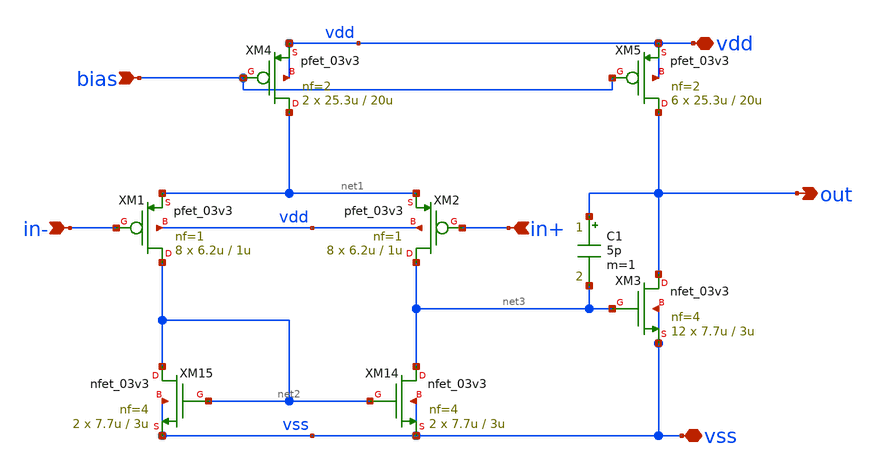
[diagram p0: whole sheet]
** sch_path: design/analog/OTA/two-stage_miller_OTA.sch
**.subckt two-stage_miller_OTA in+ in- out vdd vss bias
*.ipin in+
*.ipin in-
*.opin out
*.iopin vdd
*.iopin vss
*.ipin bias
XM1 net2 in- net1 vdd pfet_03v3 L=1u W=6.2u nf=1 ad='int((nf+1)/2) * W/nf * 0.18u' as='int((nf+2)/2) * W/nf * 0.18u'
+ pd='2*int((nf+1)/2) * (W/nf + 0.18u)' ps='2*int((nf+2)/2) * (W/nf + 0.18u)' nrd='0.18u / W' nrs='0.18u / W'
+ sa=0 sb=0 sd=0 m=8
XM2 net3 in+ net1 vdd pfet_03v3 L=1u W=6.2u nf=1 ad='int((nf+1)/2) * W/nf * 0.18u' as='int((nf+2)/2) * W/nf * 0.18u'
+ pd='2*int((nf+1)/2) * (W/nf + 0.18u)' ps='2*int((nf+2)/2) * (W/nf + 0.18u)' nrd='0.18u / W' nrs='0.18u / W'
+ sa=0 sb=0 sd=0 m=8
XM14 net3 net2 vss vss nfet_03v3 L=3u W=7.7u nf=4 ad='int((nf+1)/2) * W/nf * 0.18u' as='int((nf+2)/2) * W/nf * 0.18u'
+ pd='2*int((nf+1)/2) * (W/nf + 0.18u)' ps='2*int((nf+2)/2) * (W/nf + 0.18u)' nrd='0.18u / W' nrs='0.18u / W'
+ sa=0 sb=0 sd=0 m=2
XM15 net2 net2 vss vss nfet_03v3 L=3u W=7.7u nf=4 ad='int((nf+1)/2) * W/nf * 0.18u' as='int((nf+2)/2) * W/nf * 0.18u'
+ pd='2*int((nf+1)/2) * (W/nf + 0.18u)' ps='2*int((nf+2)/2) * (W/nf + 0.18u)' nrd='0.18u / W' nrs='0.18u / W'
+ sa=0 sb=0 sd=0 m=2
XM3 out net3 vss vss nfet_03v3 L=3u W=7.7u nf=4 ad='int((nf+1)/2) * W/nf * 0.18u' as='int((nf+2)/2) * W/nf * 0.18u'
+ pd='2*int((nf+1)/2) * (W/nf + 0.18u)' ps='2*int((nf+2)/2) * (W/nf + 0.18u)' nrd='0.18u / W' nrs='0.18u / W'
+ sa=0 sb=0 sd=0 m=12
C1 out net3 5p m=1
XM4 net1 bias vdd vdd pfet_03v3 L=20u W=25.3u nf=2 ad='int((nf+1)/2) * W/nf * 0.18u' as='int((nf+2)/2) * W/nf * 0.18u'
+ pd='2*int((nf+1)/2) * (W/nf + 0.18u)' ps='2*int((nf+2)/2) * (W/nf + 0.18u)' nrd='0.18u / W' nrs='0.18u / W'
+ sa=0 sb=0 sd=0 m=2
XM5 out bias vdd vdd pfet_03v3 L=20u W=25.3u nf=2 ad='int((nf+1)/2) * W/nf * 0.18u' as='int((nf+2)/2) * W/nf * 0.18u'
+ pd='2*int((nf+1)/2) * (W/nf + 0.18u)' ps='2*int((nf+2)/2) * (W/nf + 0.18u)' nrd='0.18u / W' nrs='0.18u / W'
+ sa=0 sb=0 sd=0 m=6
**.ends
.end
